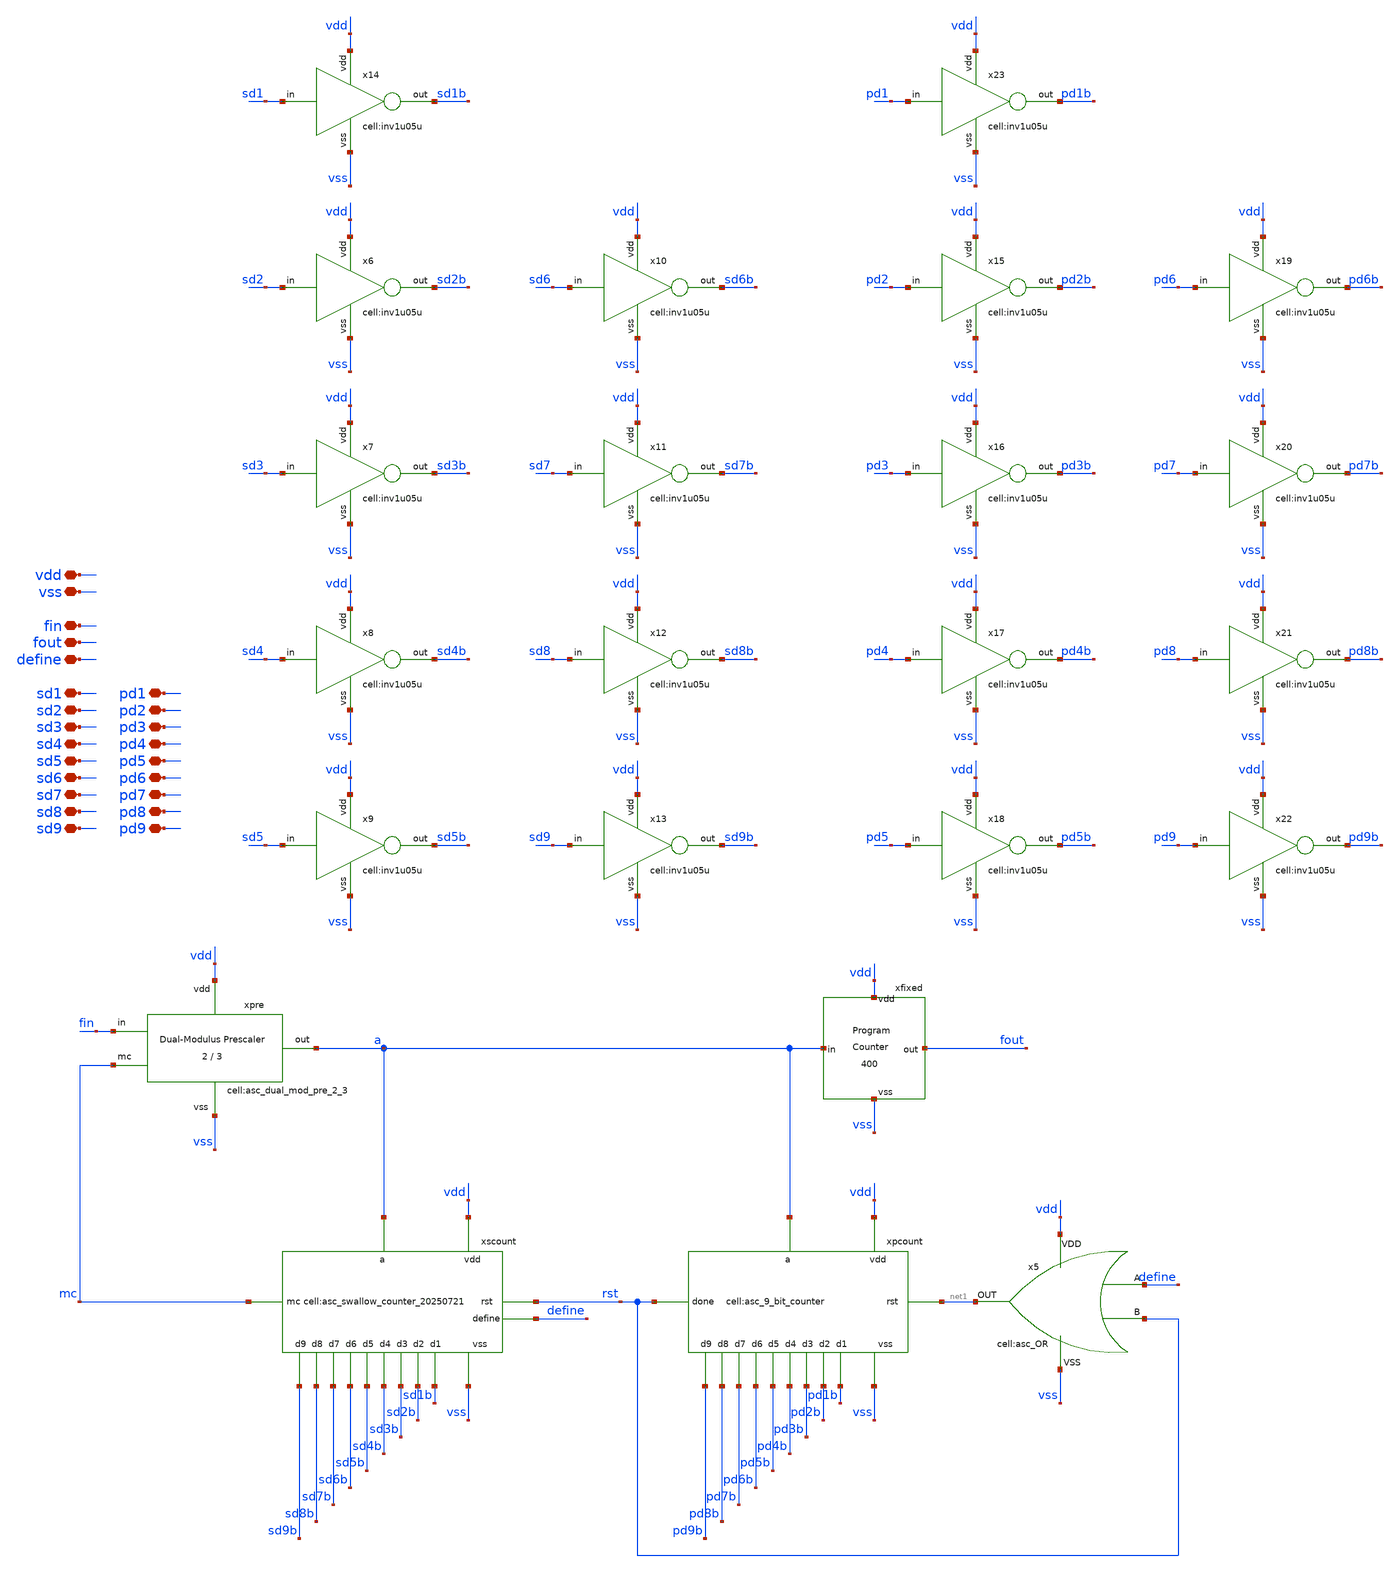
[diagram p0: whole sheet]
** sch_path: designs/libs/core_analog/asc_FM_pulse_swallow_divider_def/asc_FM_pulse_swallow_divider_def.sch
**.subckt asc_FM_pulse_swallow_divider_def vdd vss sd2 sd1 sd3 sd5 sd4 sd6 sd8 sd7 sd9 define fin
*+ fout pd2 pd1 pd3 pd5 pd4 pd6 pd8 pd7 pd9
*.iopin vdd
*.iopin vss
*.iopin sd2
*.iopin sd1
*.iopin sd3
*.iopin sd5
*.iopin sd4
*.iopin sd6
*.iopin sd8
*.iopin sd7
*.iopin sd9
*.iopin define
*.iopin fin
*.iopin fout
*.iopin pd2
*.iopin pd1
*.iopin pd3
*.iopin pd5
*.iopin pd4
*.iopin pd6
*.iopin pd8
*.iopin pd7
*.iopin pd9
xpre vdd vss a fin mc asc_dual_mod_pre_2_3
xfixed a fout vdd vss asc_program_counter_400
xscount mc sd9b sd8b sd7b sd6b sd5b sd4b sd3b sd2b sd1b vss rst vdd a define
+ asc_swallow_counter_20250721
xpcount rst pd9b pd8b pd7b pd6b pd5b pd4b pd3b pd2b pd1b vss net1 vdd a asc_9_bit_counter
x5 vdd vss net1 define rst asc_OR
x6 sd2 vdd sd2b vss inv1u05u
x7 sd3 vdd sd3b vss inv1u05u
x8 sd4 vdd sd4b vss inv1u05u
x9 sd5 vdd sd5b vss inv1u05u
x10 sd6 vdd sd6b vss inv1u05u
x11 sd7 vdd sd7b vss inv1u05u
x12 sd8 vdd sd8b vss inv1u05u
x13 sd9 vdd sd9b vss inv1u05u
x14 sd1 vdd sd1b vss inv1u05u
x15 pd2 vdd pd2b vss inv1u05u
x16 pd3 vdd pd3b vss inv1u05u
x17 pd4 vdd pd4b vss inv1u05u
x18 pd5 vdd pd5b vss inv1u05u
x19 pd6 vdd pd6b vss inv1u05u
x20 pd7 vdd pd7b vss inv1u05u
x21 pd8 vdd pd8b vss inv1u05u
x22 pd9 vdd pd9b vss inv1u05u
x23 pd1 vdd pd1b vss inv1u05u
**.ends
.end
